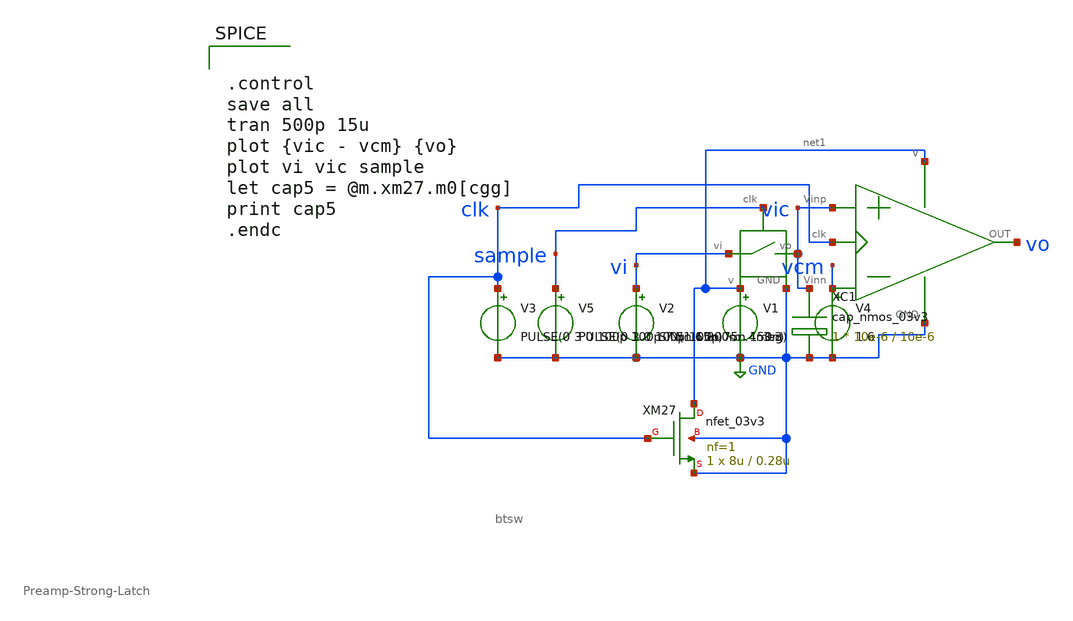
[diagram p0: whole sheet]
** sch_path: btsw/btsw_symbol.sch
**.subckt btsw_symbol
V1 net1 GND 3.3
V2 vi GND SIN(1.6 800m .4meg)
V3 clk GND PULSE(0 3 0 100p 100p 7.5n 15n)
X1 sample vi vic net1 GND btsw
V4 vcm GND 1.6
X1 net1 GND vic vcm vo clk Preamp-Strong-Latch
V5 sample GND PULSE(0 3 0 100p 100p 75n 150n)
XM27 net1 clk GND GND nfet_03v3 L=0.28u W=8u nf=1 ad='int((nf+1)/2) * W/nf * 0.18u' as='int((nf+2)/2) * W/nf * 0.18u'
+ pd='2*int((nf+1)/2) * (W/nf + 0.18u)' ps='2*int((nf+2)/2) * (W/nf + 0.18u)' nrd='0.18u / W' nrs='0.18u / W'
+ sa=0 sb=0 sd=0 m=1
XC1 vic GND cap_nmos_03v3 c_width=10e-6 c_length=10e-6 m=1
**** begin user architecture code


.control
save all
tran 500p 15u
plot {vic - vcm} {vo}
plot vi vic sample
let cap5 = @m.xm27.m0[cgg]
print cap5
.endc


.include /foss/pdks/gf180mcuC/libs.tech/ngspice/design.ngspice
.lib /foss/pdks/gf180mcuC/libs.tech/ngspice/sm141064.ngspice typical
.lib /foss/pdks/gf180mcuC/libs.tech/ngspice/sm141064.ngspice moscap_typical

**** end user architecture code
**.ends
.GLOBAL GND
.end
